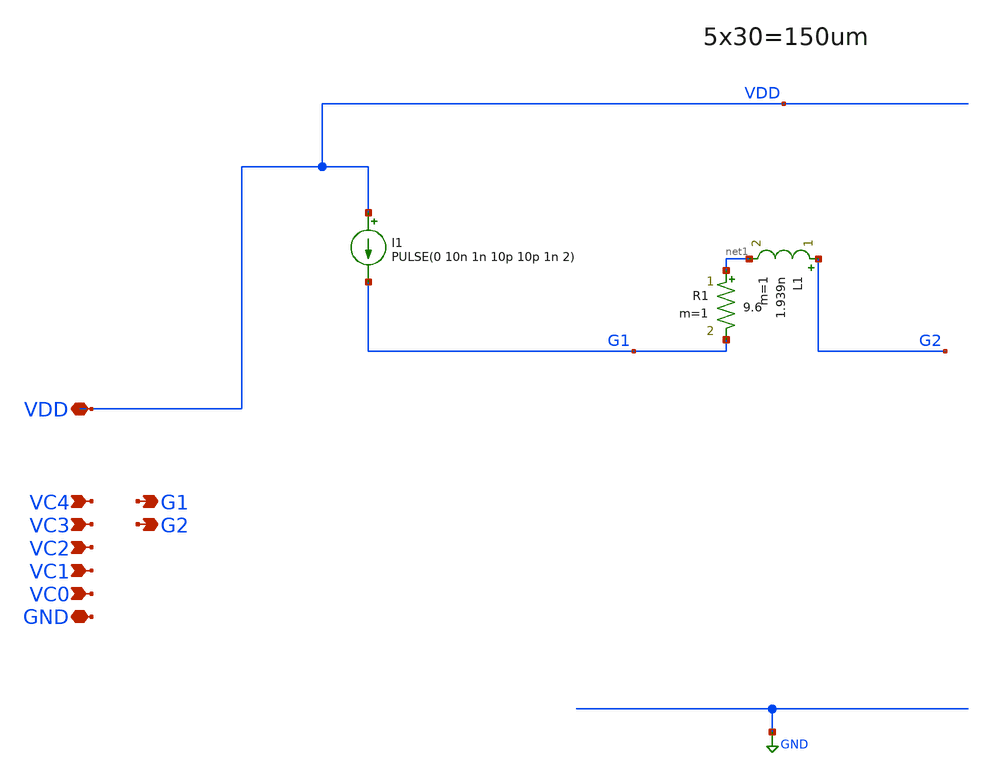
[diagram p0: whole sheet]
** sch_path: xschem/OSC_LF1_PEX_u.sch
**.subckt OSC_LF1_PEX_u VC0 VC1 VC2 VC3 VC4 GND VDD G1 G2
*.ipin VC0
*.ipin VC1
*.ipin VC2
*.ipin VC3
*.ipin VC4
*.iopin GND
*.iopin VDD
*.opin G1
*.opin G2
I1 VDD G1 PULSE(0 10n 1n 10p 10p 1n 2)
L1 G2 net1 1.939n m=1
R1 net1 G1 9.6 m=1
**** begin user architecture code






**** COMPLETE *****

.subckt COMPLETE VH VL I1 I2 G0 G1 G2 G3 G4

.subckt sky130_fd_pr__rf_pfet_01v8_aF04W5p00L0p15 DRAIN GATE SOURCE
X0 DRAIN GATE SOURCE SOURCE sky130_fd_pr__pfet_01v8 ad=2.8e+12p pd=2.112e+07u as=4.05e+12p
+ ps=3.162e+07u w=5e+06u l=150000u
X1 SOURCE GATE DRAIN SOURCE sky130_fd_pr__pfet_01v8 ad=0p pd=0u as=0p ps=0u w=5e+06u l=150000u
X2 SOURCE GATE DRAIN SOURCE sky130_fd_pr__pfet_01v8 ad=0p pd=0u as=0p ps=0u w=5e+06u l=150000u
X3 DRAIN GATE SOURCE SOURCE sky130_fd_pr__pfet_01v8 ad=0p pd=0u as=0p ps=0u w=5e+06u l=150000u
C0 DRAIN SOURCE 6.07fF
.ends

X0 I2 G0 captuner_complete_2_0/sky130_fd_pr__rf_nfet_01v8_aM04W5p00L0p15_fingered_0/S VL
+ sky130_fd_pr__nfet_01v8 ad=0p pd=0u as=0p ps=0u w=5.05e+06u l=150000u
X1 I2 G0 captuner_complete_2_0/sky130_fd_pr__rf_nfet_01v8_aM04W5p00L0p15_fingered_0/S VL
+ sky130_fd_pr__nfet_01v8 ad=0p pd=0u as=0p ps=0u w=5.05e+06u l=150000u
X2 captuner_complete_2_0/sky130_fd_pr__rf_nfet_01v8_aM04W5p00L0p15_fingered_0/S G0 I2 VL
+ sky130_fd_pr__nfet_01v8 ad=0p pd=0u as=0p ps=0u w=5.05e+06u l=150000u
X3 captuner_complete_2_0/sky130_fd_pr__rf_nfet_01v8_aM04W5p00L0p15_fingered_0/S G0 I2 VL
+ sky130_fd_pr__nfet_01v8 ad=0p pd=0u as=0p ps=0u w=5.05e+06u l=150000u
X4 I2 G1 captuner_complete_2_0/sky130_fd_pr__rf_nfet_01v8_aM04W5p00L0p15_fingered_1/S VL
+ sky130_fd_pr__nfet_01v8 ad=0p pd=0u as=0p ps=0u w=5.05e+06u l=150000u
X5 I2 G1 captuner_complete_2_0/sky130_fd_pr__rf_nfet_01v8_aM04W5p00L0p15_fingered_1/S VL
+ sky130_fd_pr__nfet_01v8 ad=0p pd=0u as=0p ps=0u w=5.05e+06u l=150000u
X6 captuner_complete_2_0/sky130_fd_pr__rf_nfet_01v8_aM04W5p00L0p15_fingered_1/S G1 I2 VL
+ sky130_fd_pr__nfet_01v8 ad=0p pd=0u as=0p ps=0u w=5.05e+06u l=150000u
X7 captuner_complete_2_0/sky130_fd_pr__rf_nfet_01v8_aM04W5p00L0p15_fingered_1/S G1 I2 VL
+ sky130_fd_pr__nfet_01v8 ad=0p pd=0u as=0p ps=0u w=5.05e+06u l=150000u
X8 I2 G2 captuner_complete_2_0/sky130_fd_pr__rf_nfet_01v8_aM04W5p00L0p15_fingered_2/S VL
+ sky130_fd_pr__nfet_01v8 ad=0p pd=0u as=0p ps=0u w=5.05e+06u l=150000u
X9 I2 G2 captuner_complete_2_0/sky130_fd_pr__rf_nfet_01v8_aM04W5p00L0p15_fingered_2/S VL
+ sky130_fd_pr__nfet_01v8 ad=0p pd=0u as=0p ps=0u w=5.05e+06u l=150000u
X10 captuner_complete_2_0/sky130_fd_pr__rf_nfet_01v8_aM04W5p00L0p15_fingered_2/S G2 I2 VL
+ sky130_fd_pr__nfet_01v8 ad=0p pd=0u as=0p ps=0u w=5.05e+06u l=150000u
X11 captuner_complete_2_0/sky130_fd_pr__rf_nfet_01v8_aM04W5p00L0p15_fingered_2/S G2 I2 VL
+ sky130_fd_pr__nfet_01v8 ad=0p pd=0u as=0p ps=0u w=5.05e+06u l=150000u
X12 I2 G3 captuner_complete_2_0/sky130_fd_pr__rf_nfet_01v8_aM04W5p00L0p15_fingered_4/S VL
+ sky130_fd_pr__nfet_01v8 ad=0p pd=0u as=0p ps=0u w=5.05e+06u l=150000u
X13 I2 G3 captuner_complete_2_0/sky130_fd_pr__rf_nfet_01v8_aM04W5p00L0p15_fingered_4/S VL
+ sky130_fd_pr__nfet_01v8 ad=0p pd=0u as=0p ps=0u w=5.05e+06u l=150000u
X14 captuner_complete_2_0/sky130_fd_pr__rf_nfet_01v8_aM04W5p00L0p15_fingered_4/S G3 I2 VL
+ sky130_fd_pr__nfet_01v8 ad=0p pd=0u as=0p ps=0u w=5.05e+06u l=150000u
X15 captuner_complete_2_0/sky130_fd_pr__rf_nfet_01v8_aM04W5p00L0p15_fingered_4/S G3 I2 VL
+ sky130_fd_pr__nfet_01v8 ad=0p pd=0u as=0p ps=0u w=5.05e+06u l=150000u
X16 I2 G3 captuner_complete_2_0/sky130_fd_pr__rf_nfet_01v8_aM04W5p00L0p15_fingered_4/S VL
+ sky130_fd_pr__nfet_01v8 ad=0p pd=0u as=0p ps=0u w=5.05e+06u l=150000u
X17 I2 G3 captuner_complete_2_0/sky130_fd_pr__rf_nfet_01v8_aM04W5p00L0p15_fingered_4/S VL
+ sky130_fd_pr__nfet_01v8 ad=0p pd=0u as=0p ps=0u w=5.05e+06u l=150000u
X18 captuner_complete_2_0/sky130_fd_pr__rf_nfet_01v8_aM04W5p00L0p15_fingered_4/S G3 I2 VL
+ sky130_fd_pr__nfet_01v8 ad=0p pd=0u as=0p ps=0u w=5.05e+06u l=150000u
X19 captuner_complete_2_0/sky130_fd_pr__rf_nfet_01v8_aM04W5p00L0p15_fingered_4/S G3 I2 VL
+ sky130_fd_pr__nfet_01v8 ad=0p pd=0u as=0p ps=0u w=5.05e+06u l=150000u
X20 I2 G4 captuner_complete_2_0/sky130_fd_pr__rf_nfet_01v8_aM04W5p00L0p15_fingered_6/S VL
+ sky130_fd_pr__nfet_01v8 ad=0p pd=0u as=0p ps=0u w=5.05e+06u l=150000u
X21 I2 G4 captuner_complete_2_0/sky130_fd_pr__rf_nfet_01v8_aM04W5p00L0p15_fingered_6/S VL
+ sky130_fd_pr__nfet_01v8 ad=0p pd=0u as=0p ps=0u w=5.05e+06u l=150000u
X22 captuner_complete_2_0/sky130_fd_pr__rf_nfet_01v8_aM04W5p00L0p15_fingered_6/S G4 I2 VL
+ sky130_fd_pr__nfet_01v8 ad=0p pd=0u as=0p ps=0u w=5.05e+06u l=150000u
X23 captuner_complete_2_0/sky130_fd_pr__rf_nfet_01v8_aM04W5p00L0p15_fingered_6/S G4 I2 VL
+ sky130_fd_pr__nfet_01v8 ad=0p pd=0u as=0p ps=0u w=5.05e+06u l=150000u
X24 I2 G4 captuner_complete_2_0/sky130_fd_pr__rf_nfet_01v8_aM04W5p00L0p15_fingered_6/S VL
+ sky130_fd_pr__nfet_01v8 ad=0p pd=0u as=0p ps=0u w=5.05e+06u l=150000u
X25 I2 G4 captuner_complete_2_0/sky130_fd_pr__rf_nfet_01v8_aM04W5p00L0p15_fingered_6/S VL
+ sky130_fd_pr__nfet_01v8 ad=0p pd=0u as=0p ps=0u w=5.05e+06u l=150000u
X26 captuner_complete_2_0/sky130_fd_pr__rf_nfet_01v8_aM04W5p00L0p15_fingered_6/S G4 I2 VL
+ sky130_fd_pr__nfet_01v8 ad=0p pd=0u as=0p ps=0u w=5.05e+06u l=150000u
X27 captuner_complete_2_0/sky130_fd_pr__rf_nfet_01v8_aM04W5p00L0p15_fingered_6/S G4 I2 VL
+ sky130_fd_pr__nfet_01v8 ad=0p pd=0u as=0p ps=0u w=5.05e+06u l=150000u
X28 I1 captuner_complete_2_0/sky130_fd_pr__rf_nfet_01v8_aM04W5p00L0p15_fingered_4/S
+ sky130_fd_pr__cap_mim_m3_1 l=4e+06u w=1e+07u
X29 I1 captuner_complete_2_0/sky130_fd_pr__rf_nfet_01v8_aM04W5p00L0p15_fingered_0/S
+ sky130_fd_pr__cap_mim_m3_1 l=1e+06u w=5e+06u
X30 I1 captuner_complete_2_0/sky130_fd_pr__rf_nfet_01v8_aM04W5p00L0p15_fingered_6/S
+ sky130_fd_pr__cap_mim_m3_1 l=8e+06u w=1e+07u
X31 I1 captuner_complete_2_0/sky130_fd_pr__rf_nfet_01v8_aM04W5p00L0p15_fingered_1/S
+ sky130_fd_pr__cap_mim_m3_1 l=1e+06u w=1e+07u
X32 I1 captuner_complete_2_0/sky130_fd_pr__rf_nfet_01v8_aM04W5p00L0p15_fingered_2/S
+ sky130_fd_pr__cap_mim_m3_1 l=2e+06u w=1e+07u
X33 VL I1 I2 VL sky130_fd_pr__nfet_01v8 ad=0p pd=0u as=0p ps=0u w=5.05e+06u l=150000u
X34 VL I1 I2 VL sky130_fd_pr__nfet_01v8 ad=0p pd=0u as=0p ps=0u w=5.05e+06u l=150000u
X35 I2 I1 VL VL sky130_fd_pr__nfet_01v8 ad=0p pd=0u as=0p ps=0u w=5.05e+06u l=150000u
X36 I2 I1 VL VL sky130_fd_pr__nfet_01v8 ad=0p pd=0u as=0p ps=0u w=5.05e+06u l=150000u
X37 VL I1 I2 VL sky130_fd_pr__nfet_01v8 ad=0p pd=0u as=0p ps=0u w=5.05e+06u l=150000u
X38 VL I1 I2 VL sky130_fd_pr__nfet_01v8 ad=0p pd=0u as=0p ps=0u w=5.05e+06u l=150000u
X39 I2 I1 VL VL sky130_fd_pr__nfet_01v8 ad=0p pd=0u as=0p ps=0u w=5.05e+06u l=150000u
X40 I2 I1 VL VL sky130_fd_pr__nfet_01v8 ad=0p pd=0u as=0p ps=0u w=5.05e+06u l=150000u
X41 VL I1 I2 VL sky130_fd_pr__nfet_01v8 ad=0p pd=0u as=0p ps=0u w=5.05e+06u l=150000u
X42 VL I1 I2 VL sky130_fd_pr__nfet_01v8 ad=0p pd=0u as=0p ps=0u w=5.05e+06u l=150000u
X43 I2 I1 VL VL sky130_fd_pr__nfet_01v8 ad=0p pd=0u as=0p ps=0u w=5.05e+06u l=150000u
X44 I2 I1 VL VL sky130_fd_pr__nfet_01v8 ad=0p pd=0u as=0p ps=0u w=5.05e+06u l=150000u
X45 VL I2 I1 VL sky130_fd_pr__nfet_01v8 ad=0p pd=0u as=0p ps=0u w=5.05e+06u l=150000u
X46 VL I2 I1 VL sky130_fd_pr__nfet_01v8 ad=0p pd=0u as=0p ps=0u w=5.05e+06u l=150000u
X47 I1 I2 VL VL sky130_fd_pr__nfet_01v8 ad=0p pd=0u as=0p ps=0u w=5.05e+06u l=150000u
X48 I1 I2 VL VL sky130_fd_pr__nfet_01v8 ad=0p pd=0u as=0p ps=0u w=5.05e+06u l=150000u
X49 VL I2 I1 VL sky130_fd_pr__nfet_01v8 ad=0p pd=0u as=0p ps=0u w=5.05e+06u l=150000u
X50 VL I2 I1 VL sky130_fd_pr__nfet_01v8 ad=0p pd=0u as=0p ps=0u w=5.05e+06u l=150000u
X51 I1 I2 VL VL sky130_fd_pr__nfet_01v8 ad=0p pd=0u as=0p ps=0u w=5.05e+06u l=150000u
X52 I1 I2 VL VL sky130_fd_pr__nfet_01v8 ad=0p pd=0u as=0p ps=0u w=5.05e+06u l=150000u
X53 VL I2 I1 VL sky130_fd_pr__nfet_01v8 ad=0p pd=0u as=0p ps=0u w=5.05e+06u l=150000u
X54 VL I2 I1 VL sky130_fd_pr__nfet_01v8 ad=0p pd=0u as=0p ps=0u w=5.05e+06u l=150000u
X55 I1 I2 VL VL sky130_fd_pr__nfet_01v8 ad=0p pd=0u as=0p ps=0u w=5.05e+06u l=150000u
X56 I1 I2 VL VL sky130_fd_pr__nfet_01v8 ad=0p pd=0u as=0p ps=0u w=5.05e+06u l=150000u
C0 captuner_complete_2_0/sky130_fd_pr__rf_nfet_01v8_aM04W5p00L0p15_fingered_2/S I2 10.36fF
C1 captuner_complete_2_0/sky130_fd_pr__rf_nfet_01v8_aM04W5p00L0p15_fingered_2/S I1 2.57fF
C2 I2 captuner_complete_2_0/sky130_fd_pr__rf_nfet_01v8_aM04W5p00L0p15_fingered_4/S 20.62fF
C3 I1 captuner_complete_2_0/sky130_fd_pr__rf_nfet_01v8_aM04W5p00L0p15_fingered_4/S 4.41fF
C4 G4 I2 2.69fF
C5 captuner_complete_2_0/sky130_fd_pr__rf_nfet_01v8_aM04W5p00L0p15_fingered_0/S I2 10.35fF
C6 I2 captuner_complete_2_0/sky130_fd_pr__rf_nfet_01v8_aM04W5p00L0p15_fingered_6/S 21.16fF
C7 captuner_complete_2_0/sky130_fd_pr__rf_nfet_01v8_aM04W5p00L0p15_fingered_1/S I2 10.32fF
C8 I1 captuner_complete_2_0/sky130_fd_pr__rf_nfet_01v8_aM04W5p00L0p15_fingered_6/S 8.73fF
C9 VH I2 56.20fF
C10 VH I1 56.69fF
C11 I2 I1 20.88fF
C12 I2 G3 2.54fF
Xsky130_fd_pr__cap_vpp_08p6x07p8_m1m2m3_shieldl1_0 VL VH VL
+ sky130_fd_pr__cap_vpp_08p6x07p8_m1m2m3_shieldl1
Xsky130_fd_pr__cap_vpp_08p6x07p8_m1m2m3_shieldl1_1 VL VH VL
+ sky130_fd_pr__cap_vpp_08p6x07p8_m1m2m3_shieldl1
Xsky130_fd_pr__cap_vpp_08p6x07p8_m1m2m3_shieldl1_2 VL VH VL
+ sky130_fd_pr__cap_vpp_08p6x07p8_m1m2m3_shieldl1
XXCP_1_0/RF_pfet_28xW5p0L0p15_0/sky130_fd_pr__rf_pfet_01v8_aF04W5p00L0p15_0 I2 I1  VH
+ sky130_fd_pr__rf_pfet_01v8_aF04W5p00L0p15
XXCP_1_0/RF_pfet_28xW5p0L0p15_0/sky130_fd_pr__rf_pfet_01v8_aF04W5p00L0p15_1 I2 I1  VH
+ sky130_fd_pr__rf_pfet_01v8_aF04W5p00L0p15
XXCP_1_0/RF_pfet_28xW5p0L0p15_0/sky130_fd_pr__rf_pfet_01v8_aF04W5p00L0p15_2 I2 I1  VH
+ sky130_fd_pr__rf_pfet_01v8_aF04W5p00L0p15
XXCP_1_0/RF_pfet_28xW5p0L0p15_0/sky130_fd_pr__rf_pfet_01v8_aF04W5p00L0p15_3 I2 I1  VH
+ sky130_fd_pr__rf_pfet_01v8_aF04W5p00L0p15
XXCP_1_0/RF_pfet_28xW5p0L0p15_0/sky130_fd_pr__rf_pfet_01v8_aF04W5p00L0p15_4 I2 I1  VH
+ sky130_fd_pr__rf_pfet_01v8_aF04W5p00L0p15
XXCP_1_0/RF_pfet_28xW5p0L0p15_0/sky130_fd_pr__rf_pfet_01v8_aF04W5p00L0p15_5 I2 I1  VH
+ sky130_fd_pr__rf_pfet_01v8_aF04W5p00L0p15
XXCP_1_0/RF_pfet_28xW5p0L0p15_0/sky130_fd_pr__rf_pfet_01v8_aF04W5p00L0p15_6 I2 I1  VH
+ sky130_fd_pr__rf_pfet_01v8_aF04W5p00L0p15
XXCP_1_0/RF_pfet_28xW5p0L0p15_1/sky130_fd_pr__rf_pfet_01v8_aF04W5p00L0p15_0 I1 I2  VH
+ sky130_fd_pr__rf_pfet_01v8_aF04W5p00L0p15
XXCP_1_0/RF_pfet_28xW5p0L0p15_1/sky130_fd_pr__rf_pfet_01v8_aF04W5p00L0p15_1 I1 I2  VH
+ sky130_fd_pr__rf_pfet_01v8_aF04W5p00L0p15
XXCP_1_0/RF_pfet_28xW5p0L0p15_1/sky130_fd_pr__rf_pfet_01v8_aF04W5p00L0p15_2 I1 I2  VH
+ sky130_fd_pr__rf_pfet_01v8_aF04W5p00L0p15
XXCP_1_0/RF_pfet_28xW5p0L0p15_1/sky130_fd_pr__rf_pfet_01v8_aF04W5p00L0p15_3 I1 I2  VH
+ sky130_fd_pr__rf_pfet_01v8_aF04W5p00L0p15
XXCP_1_0/RF_pfet_28xW5p0L0p15_1/sky130_fd_pr__rf_pfet_01v8_aF04W5p00L0p15_4 I1 I2  VH
+ sky130_fd_pr__rf_pfet_01v8_aF04W5p00L0p15
XXCP_1_0/RF_pfet_28xW5p0L0p15_1/sky130_fd_pr__rf_pfet_01v8_aF04W5p00L0p15_5 I1 I2  VH
+ sky130_fd_pr__rf_pfet_01v8_aF04W5p00L0p15
XXCP_1_0/RF_pfet_28xW5p0L0p15_1/sky130_fd_pr__rf_pfet_01v8_aF04W5p00L0p15_6 I1 I2  VH
+ sky130_fd_pr__rf_pfet_01v8_aF04W5p00L0p15
Xsky130_fd_pr__cap_vpp_08p6x07p8_m1m2m3_shieldl1_3 VL VH VL
+ sky130_fd_pr__cap_vpp_08p6x07p8_m1m2m3_shieldl1
C13 I1 VL 29.45fF
C14 I2 VL 45.54fF
C15 VH VL 543.94fF
C16 captuner_complete_2_0/sky130_fd_pr__rf_nfet_01v8_aM04W5p00L0p15_fingered_6/S VL 6.47fF
C17 G4 VL 5.45fF
C18 captuner_complete_2_0/sky130_fd_pr__rf_nfet_01v8_aM04W5p00L0p15_fingered_4/S VL 2.68fF
C19 G3 VL 4.98fF
C20 G2 VL 3.01fF
C21 G1 VL 2.97fF
C22 G0 VL 3.07fF

.ends

**** Instantiate ****

* XU_XCP VDD GND G1 G2 XCP
* XU_CAPTUNE G1 G2 GND VC0 VC1 VC2 VC3 VC4 CAPTUNE

XU_COMPLETE VDD GND G1 G2 VC0 VC1 VC2 VC3 VC4 COMPLETE




**** end user architecture code
**.ends
.GLOBAL GND
.end
